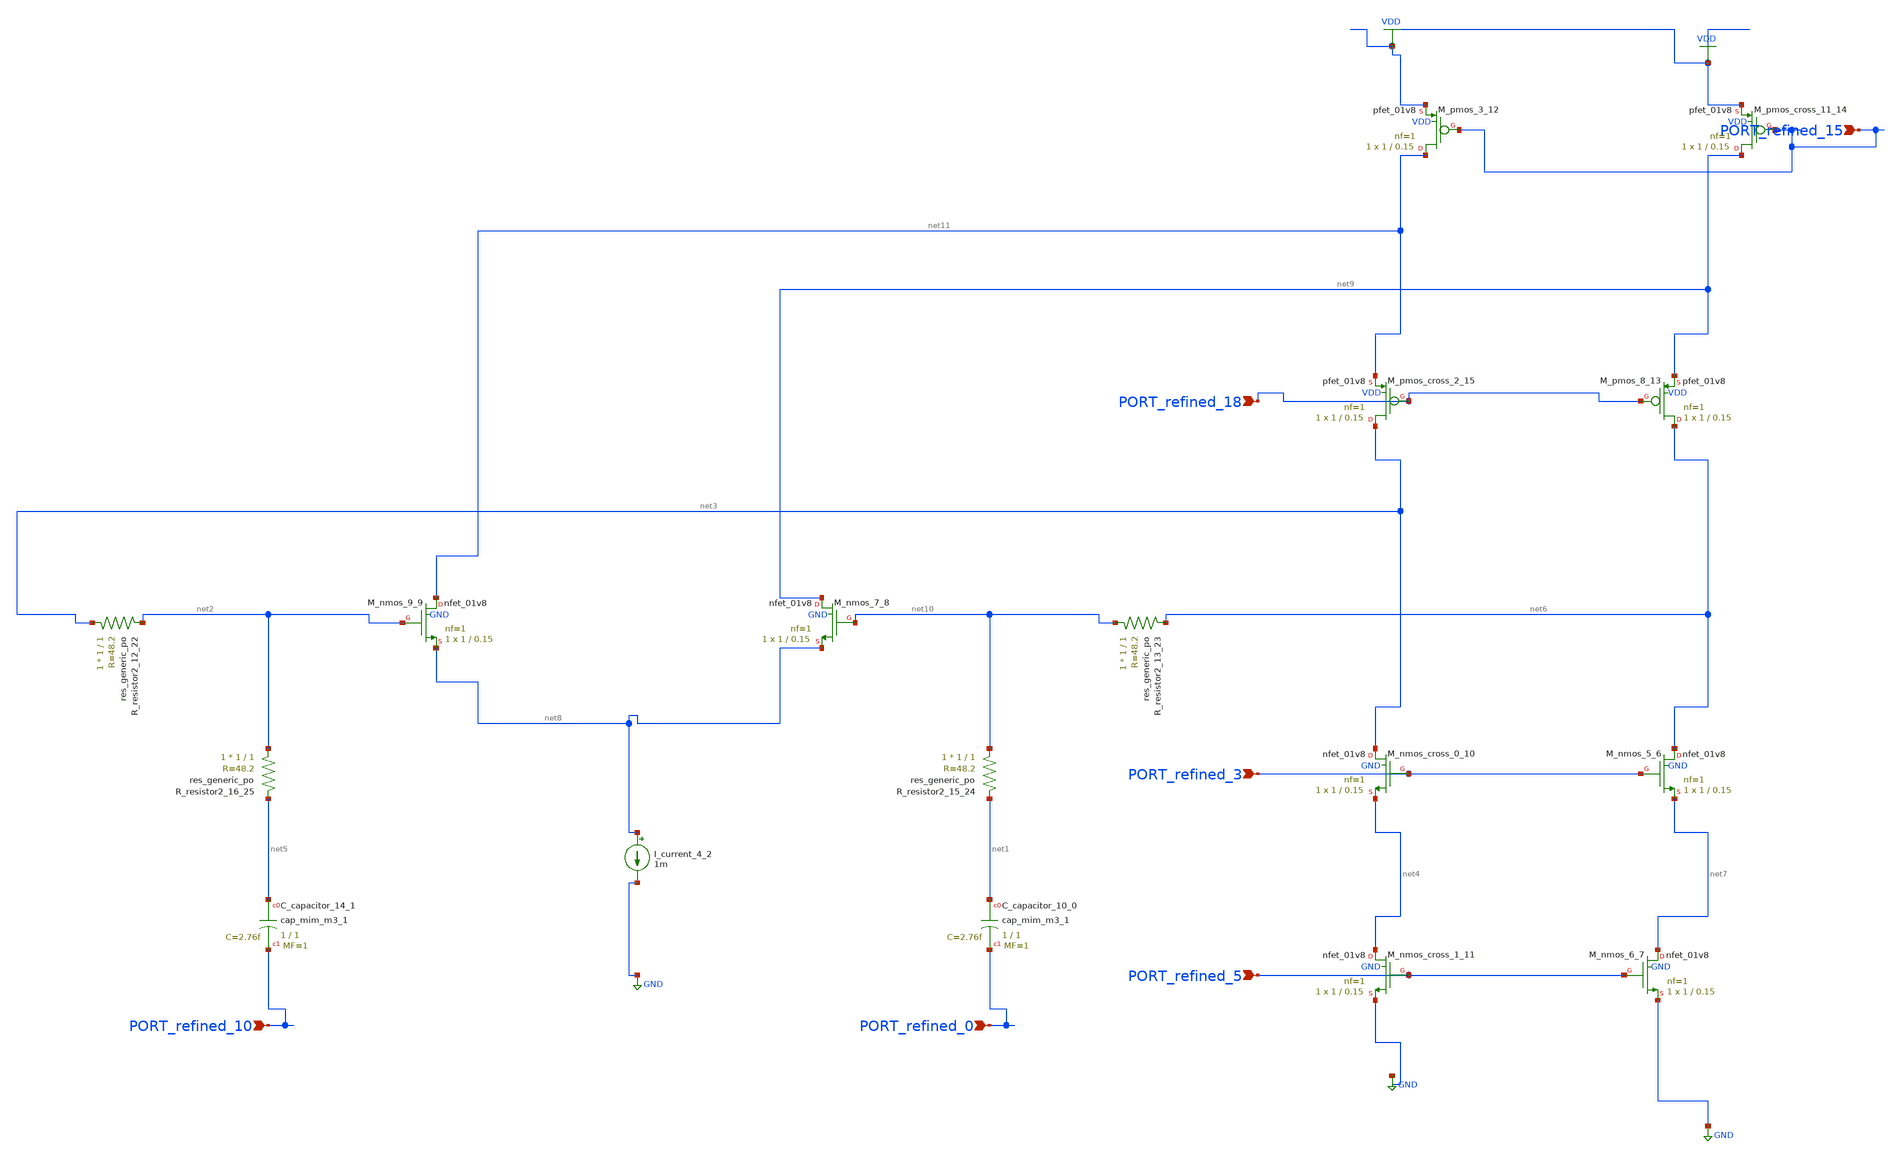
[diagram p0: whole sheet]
** sch_path: schematics/AMSNet/642.sch
**.subckt 642 PORT_refined_0 PORT_refined_10 PORT_refined_3 PORT_refined_5 PORT_refined_18
*+ PORT_refined_15
*.ipin PORT_refined_0
*.ipin PORT_refined_10
*.ipin PORT_refined_3
*.ipin PORT_refined_5
*.ipin PORT_refined_18
*.ipin PORT_refined_15
XC_capacitor_10_0 net1 PORT_refined_0 sky130_fd_pr__cap_mim_m3_1 W=1 L=1 MF=1 m=1
XC_capacitor_14_1 net5 PORT_refined_10 sky130_fd_pr__cap_mim_m3_1 W=1 L=1 MF=1 m=1
I_current_4_2 net8 GND 1m
XM_nmos_5_6 net6 PORT_refined_3 net7 GND sky130_fd_pr__nfet_01v8 L=0.15 W=1 nf=1 ad='int((1 + 1)/2) * 1 / 1 * 0.29'
+ as='int((1 + 2)/2) * 1 / 1 * 0.29' pd='2*int((1 + 1)/2) * (1 / 1 + 0.29)' ps='2*int((1 + 2)/2) * (1 / 1 + 0.29)'
+ nrd='0.29 / 1 ' nrs='0.29 / 1 ' sa=0 sb=0 sd=0 mult=1 m=1
XM_nmos_6_7 net7 PORT_refined_5 GND GND sky130_fd_pr__nfet_01v8 L=0.15 W=1 nf=1 ad='int((1 + 1)/2) * 1 / 1 * 0.29'
+ as='int((1 + 2)/2) * 1 / 1 * 0.29' pd='2*int((1 + 1)/2) * (1 / 1 + 0.29)' ps='2*int((1 + 2)/2) * (1 / 1 + 0.29)'
+ nrd='0.29 / 1 ' nrs='0.29 / 1 ' sa=0 sb=0 sd=0 mult=1 m=1
XM_nmos_7_8 net9 net10 net8 GND sky130_fd_pr__nfet_01v8 L=0.15 W=1 nf=1 ad='int((1 + 1)/2) * 1 / 1 * 0.29'
+ as='int((1 + 2)/2) * 1 / 1 * 0.29' pd='2*int((1 + 1)/2) * (1 / 1 + 0.29)' ps='2*int((1 + 2)/2) * (1 / 1 + 0.29)'
+ nrd='0.29 / 1 ' nrs='0.29 / 1 ' sa=0 sb=0 sd=0 mult=1 m=1
XM_nmos_9_9 net11 net2 net8 GND sky130_fd_pr__nfet_01v8 L=0.15 W=1 nf=1 ad='int((1 + 1)/2) * 1 / 1 * 0.29'
+ as='int((1 + 2)/2) * 1 / 1 * 0.29' pd='2*int((1 + 1)/2) * (1 / 1 + 0.29)' ps='2*int((1 + 2)/2) * (1 / 1 + 0.29)'
+ nrd='0.29 / 1 ' nrs='0.29 / 1 ' sa=0 sb=0 sd=0 mult=1 m=1
XM_nmos_cross_0_10 net3 PORT_refined_3 net4 GND sky130_fd_pr__nfet_01v8 L=0.15 W=1 nf=1 ad='int((1 + 1)/2) * 1 / 1 * 0.29'
+ as='int((1 + 2)/2) * 1 / 1 * 0.29' pd='2*int((1 + 1)/2) * (1 / 1 + 0.29)' ps='2*int((1 + 2)/2) * (1 / 1 + 0.29)'
+ nrd='0.29 / 1 ' nrs='0.29 / 1 ' sa=0 sb=0 sd=0 mult=1 m=1
XM_nmos_cross_1_11 net4 PORT_refined_5 GND GND sky130_fd_pr__nfet_01v8 L=0.15 W=1 nf=1 ad='int((1 + 1)/2) * 1 / 1 * 0.29'
+ as='int((1 + 2)/2) * 1 / 1 * 0.29' pd='2*int((1 + 1)/2) * (1 / 1 + 0.29)' ps='2*int((1 + 2)/2) * (1 / 1 + 0.29)'
+ nrd='0.29 / 1 ' nrs='0.29 / 1 ' sa=0 sb=0 sd=0 mult=1 m=1
XM_pmos_3_12 net11 PORT_refined_15 VDD VDD sky130_fd_pr__pfet_01v8 L=0.15 W=1 nf=1 ad='int((1 + 1)/2) * 1 / 1 * 0.29'
+ as='int((1 + 2)/2) * 1 / 1 * 0.29' pd='2*int((1 + 1)/2) * (1 / 1 + 0.29)' ps='2*int((1 + 2)/2) * (1 / 1 + 0.29)'
+ nrd='0.29 / 1 ' nrs='0.29 / 1 ' sa=0 sb=0 sd=0 mult=1 m=1
XM_pmos_8_13 net6 PORT_refined_18 net9 VDD sky130_fd_pr__pfet_01v8 L=0.15 W=1 nf=1 ad='int((1 + 1)/2) * 1 / 1 * 0.29'
+ as='int((1 + 2)/2) * 1 / 1 * 0.29' pd='2*int((1 + 1)/2) * (1 / 1 + 0.29)' ps='2*int((1 + 2)/2) * (1 / 1 + 0.29)'
+ nrd='0.29 / 1 ' nrs='0.29 / 1 ' sa=0 sb=0 sd=0 mult=1 m=1
XM_pmos_cross_11_14 net9 PORT_refined_15 VDD VDD sky130_fd_pr__pfet_01v8 L=0.15 W=1 nf=1 ad='int((1 + 1)/2) * 1 / 1 * 0.29'
+ as='int((1 + 2)/2) * 1 / 1 * 0.29' pd='2*int((1 + 1)/2) * (1 / 1 + 0.29)' ps='2*int((1 + 2)/2) * (1 / 1 + 0.29)'
+ nrd='0.29 / 1 ' nrs='0.29 / 1 ' sa=0 sb=0 sd=0 mult=1 m=1
XM_pmos_cross_2_15 net3 PORT_refined_18 net11 VDD sky130_fd_pr__pfet_01v8 L=0.15 W=1 nf=1 ad='int((1 + 1)/2) * 1 / 1 * 0.29'
+ as='int((1 + 2)/2) * 1 / 1 * 0.29' pd='2*int((1 + 1)/2) * (1 / 1 + 0.29)' ps='2*int((1 + 2)/2) * (1 / 1 + 0.29)'
+ nrd='0.29 / 1 ' nrs='0.29 / 1 ' sa=0 sb=0 sd=0 mult=1 m=1
XR_resistor2_12_22 net3 net2 sky130_fd_pr__res_generic_po W=1 L=1 m=1
XR_resistor2_13_23 net10 net6 sky130_fd_pr__res_generic_po W=1 L=1 m=1
XR_resistor2_15_24 net10 net1 sky130_fd_pr__res_generic_po W=1 L=1 m=1
XR_resistor2_16_25 net2 net5 sky130_fd_pr__res_generic_po W=1 L=1 m=1
**.ends
.GLOBAL GND
.GLOBAL VDD
.end
